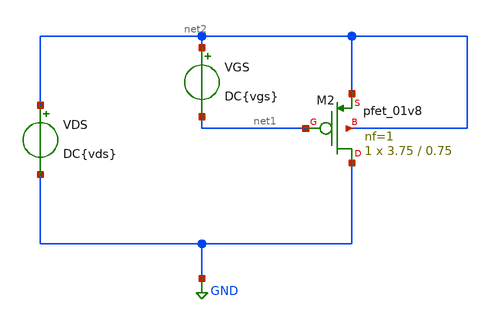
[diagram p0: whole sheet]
** sch_path: design/blocks/tp1_2/schematic/tp1_2.sch
**.subckt tp1_2
VDS net2 GND DC{vds}
XM2 GND net1 net2 net2 sky130_fd_pr__pfet_01v8 L=0.75 W=3.75 nf=1 ad='int((nf+1)/2) * W/nf * 0.29' as='int((nf+2)/2) * W/nf * 0.29'
+ pd='2*int((nf+1)/2) * (W/nf + 0.29)' ps='2*int((nf+2)/2) * (W/nf + 0.29)' nrd='0.29 / W' nrs='0.29 / W'
+ sa=0 sb=0 sd=0 mult=1 m=1
VGS net2 net1 DC{vgs}
**** begin user architecture code



* Parameters
.param vds = 1.8
.param vgs = 0.9
.options TEMPS = 27.0

* Include Models
.lib /foss/pdks/sky130A/libs.tech/ngspice/sky130.lib.spice TT
* Data to save
.save all  @M.XM2.msky130_fd_pr__pfet_01v8[id]  @M.XM2.msky130_fd_pr__pfet_01v8[gm]  @M.XM2.msky130_fd_pr__pfet_01v8[vth]  @M.XM2.msky130_fd_pr__pfet_01v8[vds]  @M.XM2.msky130_fd_pr__pfet_01v8[vdsat]  @M.XM2.msky130_fd_pr__pfet_01v8[vgs]

* Simulation
.control
  dc VDS 0 1.8 0.01 VGS 0 1.8 0.3
  setplot dc1
  plot @M.XM2.msky130_fd_pr__pfet_01v8[id] ylabel Id xlabel Vds title 'Id vs Vds vs Vgs'
  set filetype = ascii
  write tp1_2_dc1.raw

  reset
  dc VGS 0 1.8 0.01
  setplot dc2
  plot @M.XM2.msky130_fd_pr__pfet_01v8[id] ylabel Id xlabel Vgs
  set filetype = ascii
  write tp1_2_dc2.raw

.endc

.end


**** end user architecture code
**.ends
.GLOBAL GND
.end
